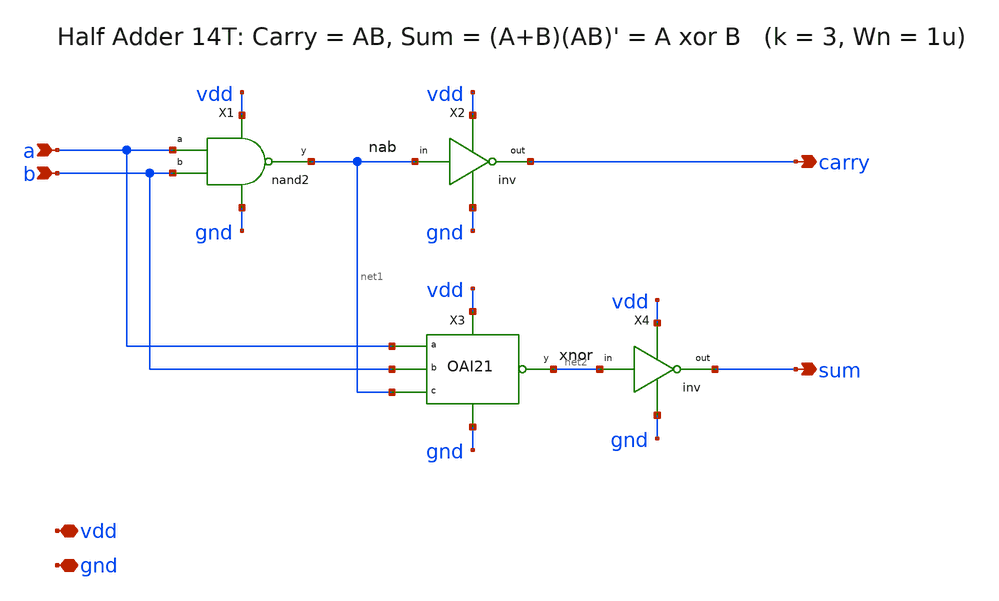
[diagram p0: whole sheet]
** sch_path: proj/xschem/ha14.sch
**.subckt ha14 a b sum carry vdd gnd
*.ipin a
*.ipin b
*.opin sum
*.opin carry
*.iopin vdd
*.iopin gnd
X1 a b net1 vdd gnd nand2
X2 net1 carry vdd gnd inv
X3 a b net1 net2 vdd gnd oai21
X4 net2 sum vdd gnd inv
**.ends

* expanding   symbol:  nand2.sym # of pins=5
** sym_path: proj/xschem/nand2.sym
** sch_path: proj/xschem/nand2.sch
.subckt nand2 a b y vdd gnd
*.ipin a
*.ipin b
*.opin y
*.iopin vdd
*.iopin gnd
XMPA y a vdd vdd sky130_fd_pr__pfet_01v8 L=0.15 W=3 nf=1 ad='int((1 + 1)/2) * 3 / 1 * 0.29' as='int((1 + 2)/2) * 3 / 1 * 0.29'
+ pd='2*int((1 + 1)/2) * (3 / 1 + 0.29)' ps='2*int((1 + 2)/2) * (3 / 1 + 0.29)' nrd='0.29 / 3 ' nrs='0.29 / 3 '
+ sa=0 sb=0 sd=0 mult=1 m=1
XMPB y b vdd vdd sky130_fd_pr__pfet_01v8 L=0.15 W=3 nf=1 ad='int((1 + 1)/2) * 3 / 1 * 0.29' as='int((1 + 2)/2) * 3 / 1 * 0.29'
+ pd='2*int((1 + 1)/2) * (3 / 1 + 0.29)' ps='2*int((1 + 2)/2) * (3 / 1 + 0.29)' nrd='0.29 / 3 ' nrs='0.29 / 3 '
+ sa=0 sb=0 sd=0 mult=1 m=1
XMNA y a net1 gnd sky130_fd_pr__nfet_01v8 L=0.15 W=2 nf=1 ad='int((nf+1)/2) * W/nf * 0.29' as='int((nf+2)/2) * W/nf * 0.29'
+ pd='2*int((nf+1)/2) * (W/nf + 0.29)' ps='2*int((nf+2)/2) * (W/nf + 0.29)' nrd='0.29 / W' nrs='0.29 / W'
+ sa=0 sb=0 sd=0 mult=1 m=1
XMNB net1 b gnd gnd sky130_fd_pr__nfet_01v8 L=0.15 W=2 nf=1 ad='int((nf+1)/2) * W/nf * 0.29' as='int((nf+2)/2) * W/nf * 0.29'
+ pd='2*int((nf+1)/2) * (W/nf + 0.29)' ps='2*int((nf+2)/2) * (W/nf + 0.29)' nrd='0.29 / W' nrs='0.29 / W'
+ sa=0 sb=0 sd=0 mult=1 m=1
.ends


* expanding   symbol:  inv.sym # of pins=4
** sym_path: proj/xschem/inv.sym
** sch_path: proj/xschem/inv.sch
.subckt inv in out vdd gnd
*.ipin in
*.opin out
*.iopin vdd
*.iopin gnd
XMP out in vdd vdd sky130_fd_pr__pfet_01v8 L=0.15 W=3 nf=1 ad='int((1 + 1)/2) * 3 / 1 * 0.29' as='int((1 + 2)/2) * 3 / 1 * 0.29'
+ pd='2*int((1 + 1)/2) * (3 / 1 + 0.29)' ps='2*int((1 + 2)/2) * (3 / 1 + 0.29)' nrd='0.29 / 3 ' nrs='0.29 / 3 '
+ sa=0 sb=0 sd=0 mult=1 m=1
XMN out in gnd gnd sky130_fd_pr__nfet_01v8 L=0.15 W=1 nf=1 ad='int((nf+1)/2) * W/nf * 0.29' as='int((nf+2)/2) * W/nf * 0.29'
+ pd='2*int((nf+1)/2) * (W/nf + 0.29)' ps='2*int((nf+2)/2) * (W/nf + 0.29)' nrd='0.29 / W' nrs='0.29 / W'
+ sa=0 sb=0 sd=0 mult=1 m=1
.ends


* expanding   symbol:  oai21.sym # of pins=6
** sym_path: proj/xschem/oai21.sym
** sch_path: proj/xschem/oai21.sch
.subckt oai21 a b c y vdd gnd
*.ipin a
*.ipin b
*.ipin c
*.opin y
*.iopin vdd
*.iopin gnd
XMPC y c vdd vdd sky130_fd_pr__pfet_01v8 L=0.15 W=3 nf=1 ad='int((1 + 1)/2) * 3 / 1 * 0.29' as='int((1 + 2)/2) * 3 / 1 * 0.29'
+ pd='2*int((1 + 1)/2) * (3 / 1 + 0.29)' ps='2*int((1 + 2)/2) * (3 / 1 + 0.29)' nrd='0.29 / 3 ' nrs='0.29 / 3 '
+ sa=0 sb=0 sd=0 mult=1 m=1
XMPA net1 a vdd vdd sky130_fd_pr__pfet_01v8 L=0.15 W=6 nf=1 ad='int((1 + 1)/2) * 6 / 1 * 0.29' as='int((1 + 2)/2) * 6 / 1 * 0.29'
+ pd='2*int((1 + 1)/2) * (6 / 1 + 0.29)' ps='2*int((1 + 2)/2) * (6 / 1 + 0.29)' nrd='0.29 / 6 ' nrs='0.29 / 6 '
+ sa=0 sb=0 sd=0 mult=1 m=1
XMPB y b net1 vdd sky130_fd_pr__pfet_01v8 L=0.15 W=6 nf=1 ad='int((1 + 1)/2) * 6 / 1 * 0.29' as='int((1 + 2)/2) * 6 / 1 * 0.29'
+ pd='2*int((1 + 1)/2) * (6 / 1 + 0.29)' ps='2*int((1 + 2)/2) * (6 / 1 + 0.29)' nrd='0.29 / 6 ' nrs='0.29 / 6 '
+ sa=0 sb=0 sd=0 mult=1 m=1
XMNC y c net2 gnd sky130_fd_pr__nfet_01v8 L=0.15 W=2 nf=1 ad='int((nf+1)/2) * W/nf * 0.29' as='int((nf+2)/2) * W/nf * 0.29'
+ pd='2*int((nf+1)/2) * (W/nf + 0.29)' ps='2*int((nf+2)/2) * (W/nf + 0.29)' nrd='0.29 / W' nrs='0.29 / W'
+ sa=0 sb=0 sd=0 mult=1 m=1
XMNA net2 a gnd gnd sky130_fd_pr__nfet_01v8 L=0.15 W=2 nf=1 ad='int((nf+1)/2) * W/nf * 0.29' as='int((nf+2)/2) * W/nf * 0.29'
+ pd='2*int((nf+1)/2) * (W/nf + 0.29)' ps='2*int((nf+2)/2) * (W/nf + 0.29)' nrd='0.29 / W' nrs='0.29 / W'
+ sa=0 sb=0 sd=0 mult=1 m=1
XMNB net2 b gnd gnd sky130_fd_pr__nfet_01v8 L=0.15 W=2 nf=1 ad='int((nf+1)/2) * W/nf * 0.29' as='int((nf+2)/2) * W/nf * 0.29'
+ pd='2*int((nf+1)/2) * (W/nf + 0.29)' ps='2*int((nf+2)/2) * (W/nf + 0.29)' nrd='0.29 / W' nrs='0.29 / W'
+ sa=0 sb=0 sd=0 mult=1 m=1
.ends

.end
